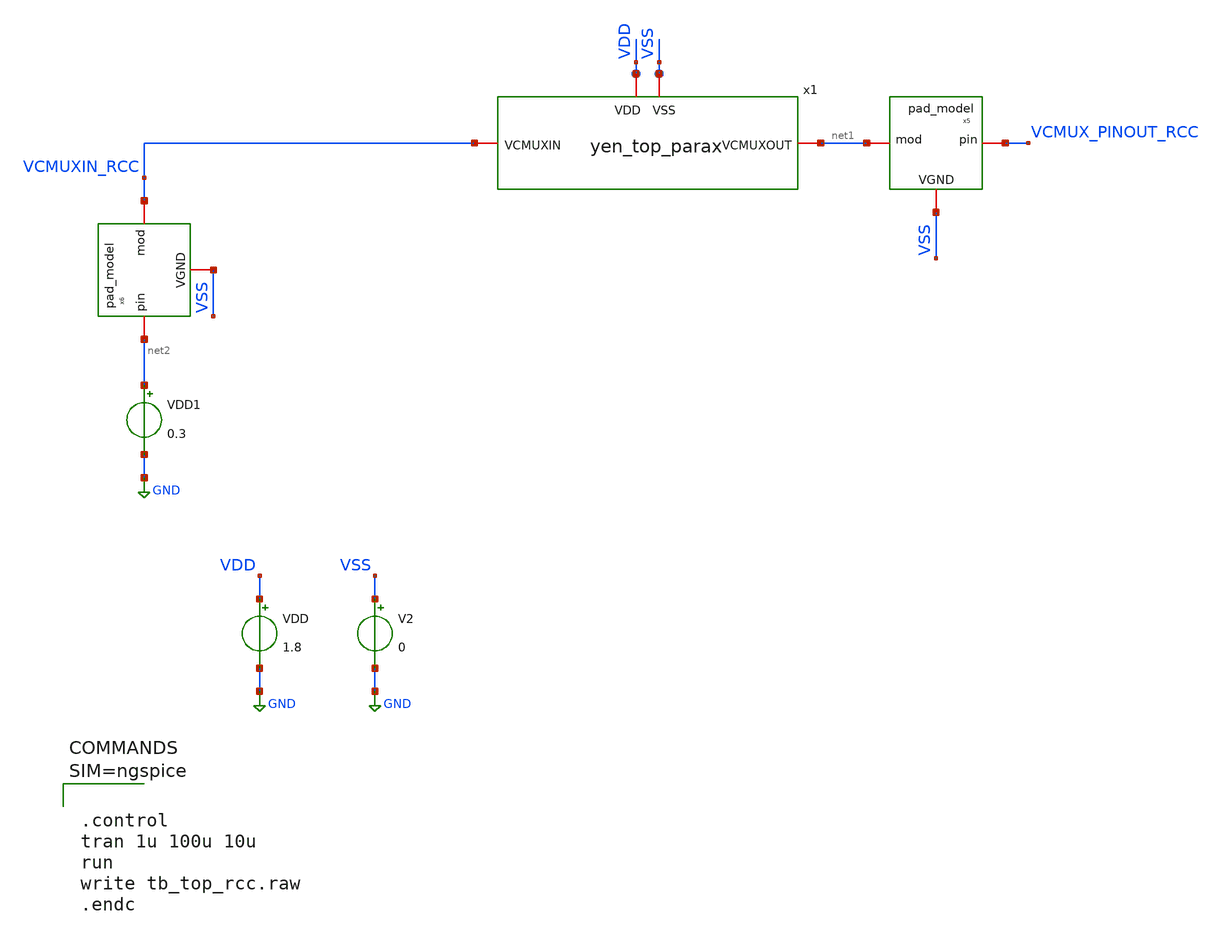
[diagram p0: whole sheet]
** sch_path: xschem/tb_top_rcc.sch
**.subckt tb_top_rcc
V2 VSS GND 0
VDD VDD GND 1.8
x1 VDD VSS VCMUXIN_RCC net1 yen_top_parax
x5 VSS VCMUX_PINOUT_RCC net1 pad_model
x6 VSS net2 VCMUXIN_RCC pad_model
VDD1 net2 GND 0.3
**** begin user architecture code

** opencircuitdesign pdks install
.lib $::SKYWATER_MODELS/sky130.lib.spice ff





.control
tran 1u 100u 10u
run
write tb_top_rcc.raw
.endc



**** end user architecture code
**.ends
.GLOBAL GND
.end
